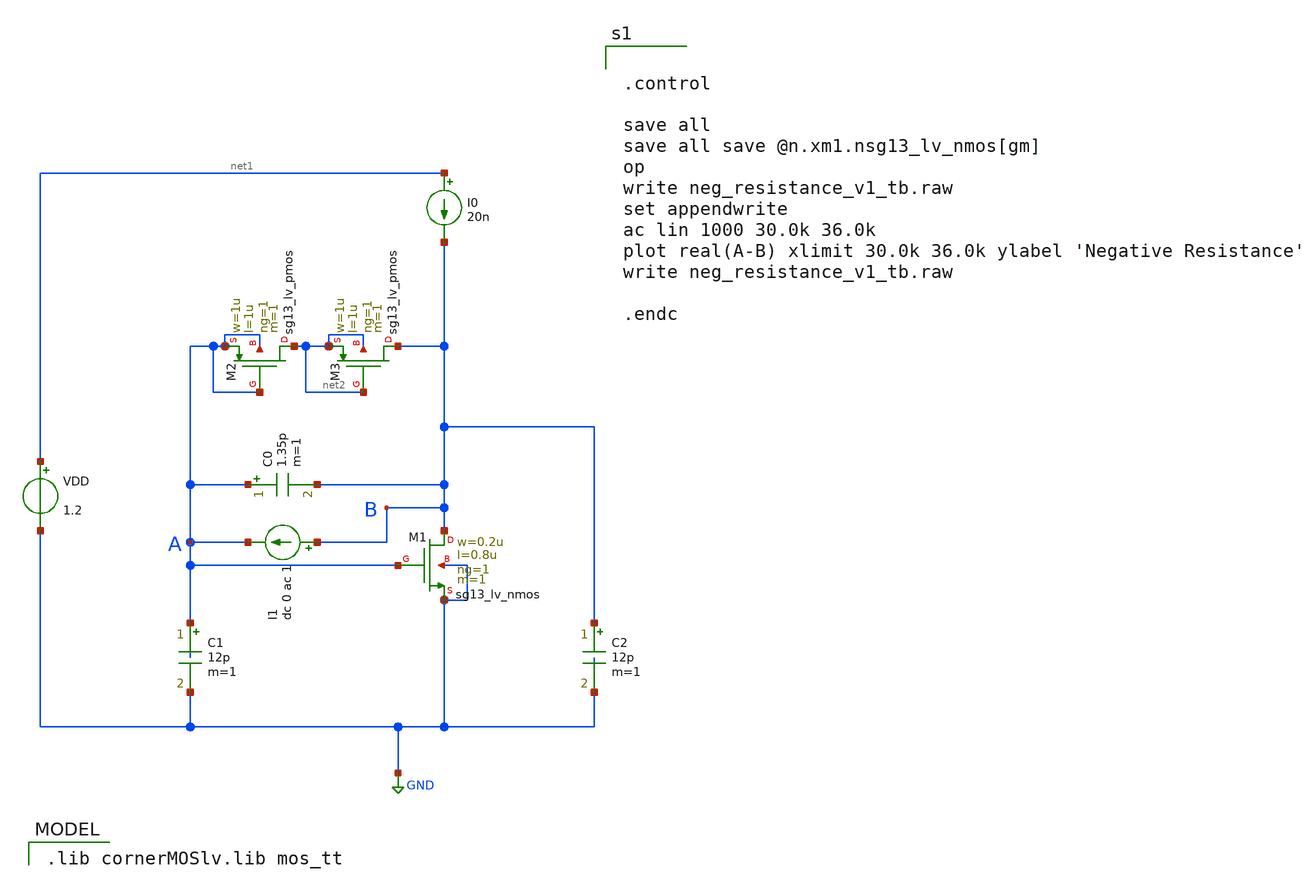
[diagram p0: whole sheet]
** sch_path: neg_resistance_v1_tb.sch
**.subckt neg_resistance_v1_tb
XM1 B A GND GND sg13_lv_nmos w=0.2u l=0.8u ng=1 m=1 mm_ok=1
C1 A GND 12p m=1
C2 B GND 12p m=1
C0 A B 1.35p m=1
I0 net1 B 20n
VDD net1 GND 1.2
I1 B A dc 0 ac 1
XM2 net2 A A A sg13_lv_pmos w=1u l=1u ng=1 m=1 mm_ok=1
XM3 B net2 net2 net2 sg13_lv_pmos w=1u l=1u ng=1 m=1 mm_ok=1
**** begin user architecture code


.control

save all
save all save @n.xm1.nsg13_lv_nmos[gm]
op
write neg_resistance_v1_tb.raw
set appendwrite
ac lin 1000 30.0k 36.0k
plot real(A-B) xlimit 30.0k 36.0k ylabel 'Negative Resistance'
write neg_resistance_v1_tb.raw

.endc


 .lib cornerMOSlv.lib mos_tt

**** end user architecture code
**.ends
.GLOBAL GND
.end
